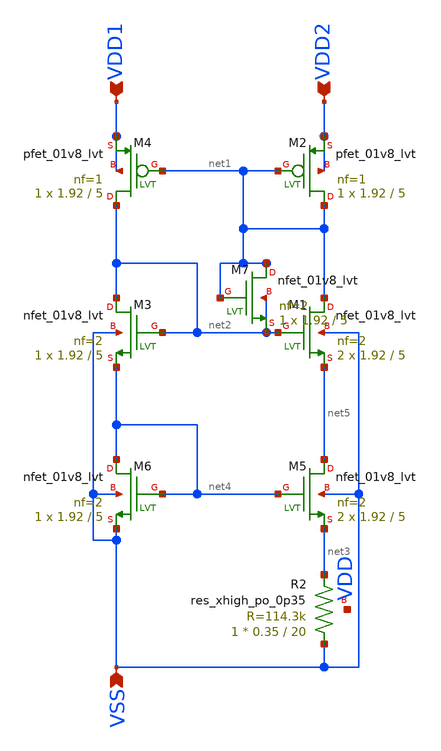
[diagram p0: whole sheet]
** sch_path: design/LELO_SVOD_SKY130A/LELO_PTAT_CURRENT.sch
**.subckt LELO_PTAT_CURRENT VDD1 VSS VDD2
*.ipin VDD1
*.ipin VSS
*.ipin VDD2
XM1 net1 net2 net5 VSS sky130_fd_pr__nfet_01v8_lvt L=5 W=1.92 nf=2 ad='int((2 + 1)/2) * 1.92 / 2 * 0.29'
+ as='int((2 + 2)/2) * 1.92 / 2 * 0.29' pd='2*int((2 + 1)/2) * (1.92 / 2 + 0.29)' ps='2*int((2 + 2)/2) * (1.92 / 2 + 0.29)'
+ nrd='0.29 / 1.92 ' nrs='0.29 / 1.92 ' sa=0 sb=0 sd=0 mult=2 m=2
XM2 net1 net1 VDD2 VDD2 sky130_fd_pr__pfet_01v8_lvt L=5 W=1.92 nf=1 ad='int((1 + 1)/2) * 1.92 / 1 * 0.29'
+ as='int((1 + 2)/2) * 1.92 / 1 * 0.29' pd='2*int((1 + 1)/2) * (1.92 / 1 + 0.29)' ps='2*int((1 + 2)/2) * (1.92 / 1 + 0.29)'
+ nrd='0.29 / 1.92 ' nrs='0.29 / 1.92 ' sa=0 sb=0 sd=0 mult=1 m=1
XM3 net2 net2 net4 VSS sky130_fd_pr__nfet_01v8_lvt L=5 W=1.92 nf=2 ad='int((2 + 1)/2) * 1.92 / 2 * 0.29'
+ as='int((2 + 2)/2) * 1.92 / 2 * 0.29' pd='2*int((2 + 1)/2) * (1.92 / 2 + 0.29)' ps='2*int((2 + 2)/2) * (1.92 / 2 + 0.29)'
+ nrd='0.29 / 1.92 ' nrs='0.29 / 1.92 ' sa=0 sb=0 sd=0 mult=1 m=1
XM4 net2 net1 VDD1 VDD1 sky130_fd_pr__pfet_01v8_lvt L=5 W=1.92 nf=1 ad='int((1 + 1)/2) * 1.92 / 1 * 0.29'
+ as='int((1 + 2)/2) * 1.92 / 1 * 0.29' pd='2*int((1 + 1)/2) * (1.92 / 1 + 0.29)' ps='2*int((1 + 2)/2) * (1.92 / 1 + 0.29)'
+ nrd='0.29 / 1.92 ' nrs='0.29 / 1.92 ' sa=0 sb=0 sd=0 mult=1 m=1
XM5 net5 net4 net3 VSS sky130_fd_pr__nfet_01v8_lvt L=5 W=1.92 nf=2 ad='int((2 + 1)/2) * 1.92 / 2 * 0.29'
+ as='int((2 + 2)/2) * 1.92 / 2 * 0.29' pd='2*int((2 + 1)/2) * (1.92 / 2 + 0.29)' ps='2*int((2 + 2)/2) * (1.92 / 2 + 0.29)'
+ nrd='0.29 / 1.92 ' nrs='0.29 / 1.92 ' sa=0 sb=0 sd=0 mult=2 m=2
XM6 net4 net4 VSS VSS sky130_fd_pr__nfet_01v8_lvt L=5 W=1.92 nf=2 ad='int((2 + 1)/2) * 1.92 / 2 * 0.29'
+ as='int((2 + 2)/2) * 1.92 / 2 * 0.29' pd='2*int((2 + 1)/2) * (1.92 / 2 + 0.29)' ps='2*int((2 + 2)/2) * (1.92 / 2 + 0.29)'
+ nrd='0.29 / 1.92 ' nrs='0.29 / 1.92 ' sa=0 sb=0 sd=0 mult=1 m=1
XM7 net1 net1 net2 net2 sky130_fd_pr__nfet_01v8_lvt L=5 W=1.92 nf=2 ad='int((2 + 1)/2) * 1.92 / 2 * 0.29'
+ as='int((2 + 2)/2) * 1.92 / 2 * 0.29' pd='2*int((2 + 1)/2) * (1.92 / 2 + 0.29)' ps='2*int((2 + 2)/2) * (1.92 / 2 + 0.29)'
+ nrd='0.29 / 1.92 ' nrs='0.29 / 1.92 ' sa=0 sb=0 sd=0 mult=1 m=1
XR2 VSS net3 VDD sky130_fd_pr__res_xhigh_po_0p35 L=20 mult=1 m=1
**.ends
.end
